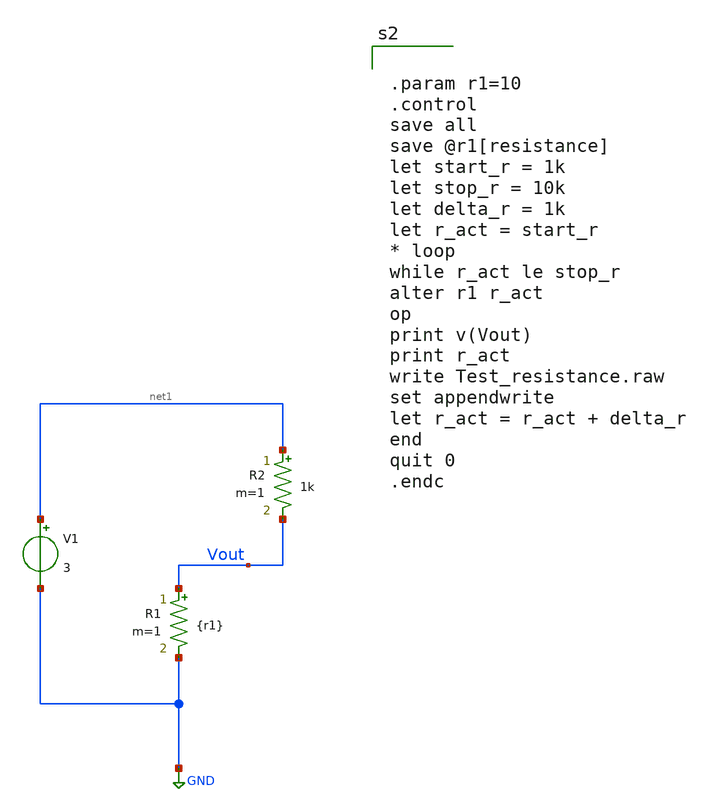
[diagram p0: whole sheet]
** sch_path: Test_resistance.sch
**.subckt Test_resistance
R1 Vout GND {r1} m=1
R2 net1 Vout 1k m=1
V1 net1 GND 3
**** begin user architecture code

** opencircuitdesign pdks install
.lib $::SKYWATER_MODELS/sky130.lib.spice tt



.param r1=10
.control
save all
save @r1[resistance]
let start_r = 1k
let stop_r = 10k
let delta_r = 1k
let r_act = start_r
* loop
while r_act le stop_r
alter r1 r_act
op
print v(Vout)
print r_act
write Test_resistance.raw
set appendwrite
let r_act = r_act + delta_r
end
quit 0
.endc


**** end user architecture code
**.ends
.GLOBAL GND
.end
